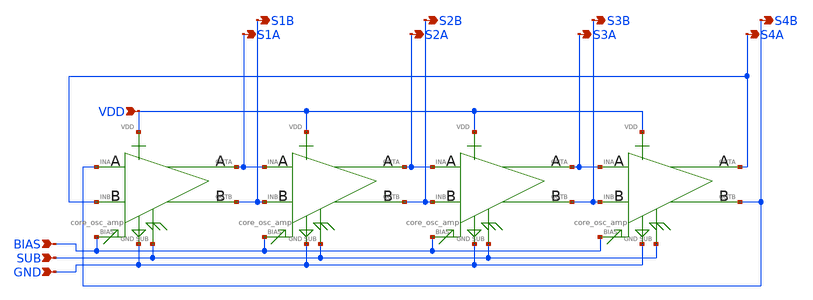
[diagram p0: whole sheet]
** sch_path: xschem/core_osc.sch
**.subckt core_osc VDD BIAS SUB GND S1A S1B S2A S2B S3A S3B S4A S4B
*.ipin VDD
*.ipin BIAS
*.ipin SUB
*.ipin GND
*.opin S1A
*.opin S1B
*.opin S2A
*.opin S2B
*.opin S3A
*.opin S3B
*.opin S4A
*.opin S4B
X1 S4B S4A BIAS VDD GND SUB S1A S1B core_osc_amp
X2 S1A S1B BIAS VDD GND SUB S2A S2B core_osc_amp
X3 S2A S2B BIAS VDD GND SUB S3A S3B core_osc_amp
X4 S3A S3B BIAS VDD GND SUB S4A S4B core_osc_amp
**.ends

* expanding   symbol:  core_osc_amp.sym # of pins=8
** sym_path: core_osc_amp.sym
** sch_path: core_osc_amp.sch
.subckt core_osc_amp INA INB BIAS VDD GND SUB OUTA OUTB
*.ipin INA
*.ipin INB
*.ipin BIAS
*.ipin GND
*.ipin VDD
*.ipin SUB
*.opin OUTA
*.opin OUTB
XM2 OUTA INA net1 SUB sky130_fd_pr__nfet_01v8_lvt L=0.15 W=4 nf=4 ad='int((nf+1)/2) * W/nf * 0.29' as='int((nf+2)/2) * W/nf * 0.29'
+ pd='2*int((nf+1)/2) * (W/nf + 0.29)' ps='2*int((nf+2)/2) * (W/nf + 0.29)' nrd='0.29 / W' nrs='0.29 / W'
+ sa=0 sb=0 sd=0 mult=1 m=1
XM3 OUTB INB net1 SUB sky130_fd_pr__nfet_01v8_lvt L=0.15 W=4 nf=4 ad='int((nf+1)/2) * W/nf * 0.29' as='int((nf+2)/2) * W/nf * 0.29'
+ pd='2*int((nf+1)/2) * (W/nf + 0.29)' ps='2*int((nf+2)/2) * (W/nf + 0.29)' nrd='0.29 / W' nrs='0.29 / W'
+ sa=0 sb=0 sd=0 mult=1 m=1
XM1 net1 BIAS GND SUB sky130_fd_pr__nfet_01v8_lvt L=0.15 W=20 nf=20 ad='int((nf+1)/2) * W/nf * 0.29'
+ as='int((nf+2)/2) * W/nf * 0.29' pd='2*int((nf+1)/2) * (W/nf + 0.29)' ps='2*int((nf+2)/2) * (W/nf + 0.29)'
+ nrd='0.29 / W' nrs='0.29 / W' sa=0 sb=0 sd=0 mult=1 m=1
XR16 OUTA VDD SUB sky130_fd_pr__res_high_po_2p85 L=7.6 mult=1 m=1
XR17 OUTB VDD SUB sky130_fd_pr__res_high_po_2p85 L=7.6 mult=1 m=1
XM4 net1 BIAS GND SUB sky130_fd_pr__nfet_01v8_lvt L=0.15 W=20 nf=20 ad='int((nf+1)/2) * W/nf * 0.29'
+ as='int((nf+2)/2) * W/nf * 0.29' pd='2*int((nf+1)/2) * (W/nf + 0.29)' ps='2*int((nf+2)/2) * (W/nf + 0.29)'
+ nrd='0.29 / W' nrs='0.29 / W' sa=0 sb=0 sd=0 mult=1 m=1
.ends

.end
